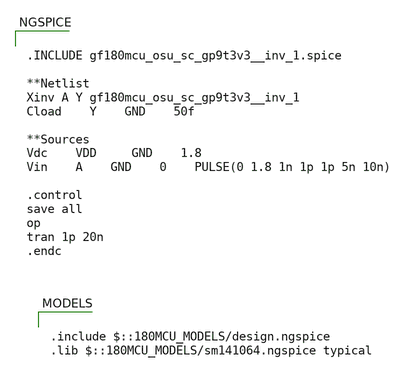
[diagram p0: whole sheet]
** sch_path: xschem/test_bench_inv.sch
**.subckt test_bench_inv
**** begin user architecture code


.INCLUDE gf180mcu_osu_sc_gp9t3v3__inv_1.spice

**Netlist
Xinv A Y gf180mcu_osu_sc_gp9t3v3__inv_1
Cload	Y	GND	50f

**Sources
Vdc	VDD 	GND	1.8
Vin	A	GND	0	PULSE(0 1.8 1n 1p 1p 5n 10n)

.control
save all
op
tran 1p 20n
.endc



.include $::180MCU_MODELS/design.ngspice
.lib $::180MCU_MODELS/sm141064.ngspice typical

**** end user architecture code
**.ends
.end
